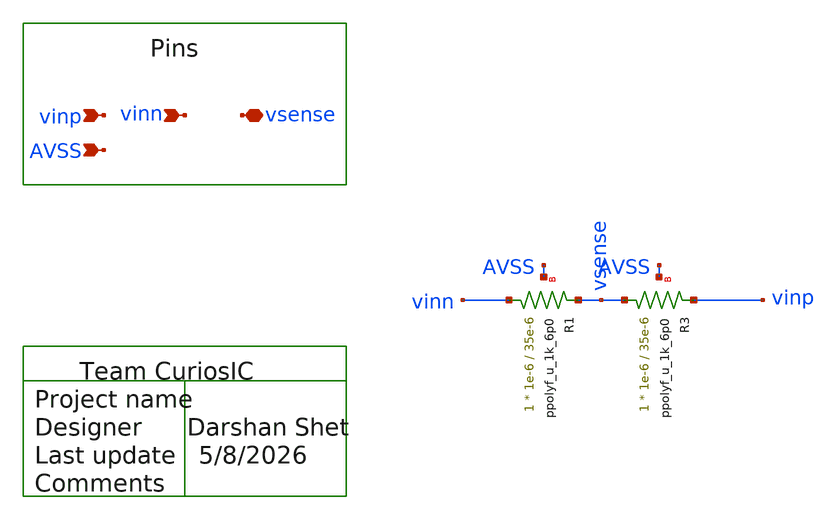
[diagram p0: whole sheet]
** sch_path: design/schematics/ADC/DSM_Loop_filter/First_int/OTA_Files/DS_cic_bms_afe_iadc_first_int_OTA_CMFB_resistor_divider.sch
**.subckt DS_cic_bms_afe_iadc_first_int_OTA_CMFB_resistor_divider vinp vinn vsense AVSS
*.ipin vinp
*.ipin vinn
*.iopin vsense
*.ipin AVSS
XR1 vinn vsense AVSS ppolyf_u_1k_6p0 r_width=1e-6 r_length=35e-6 m=1
XR3 vsense vinp AVSS ppolyf_u_1k_6p0 r_width=1e-6 r_length=35e-6 m=1
**.ends
.end
